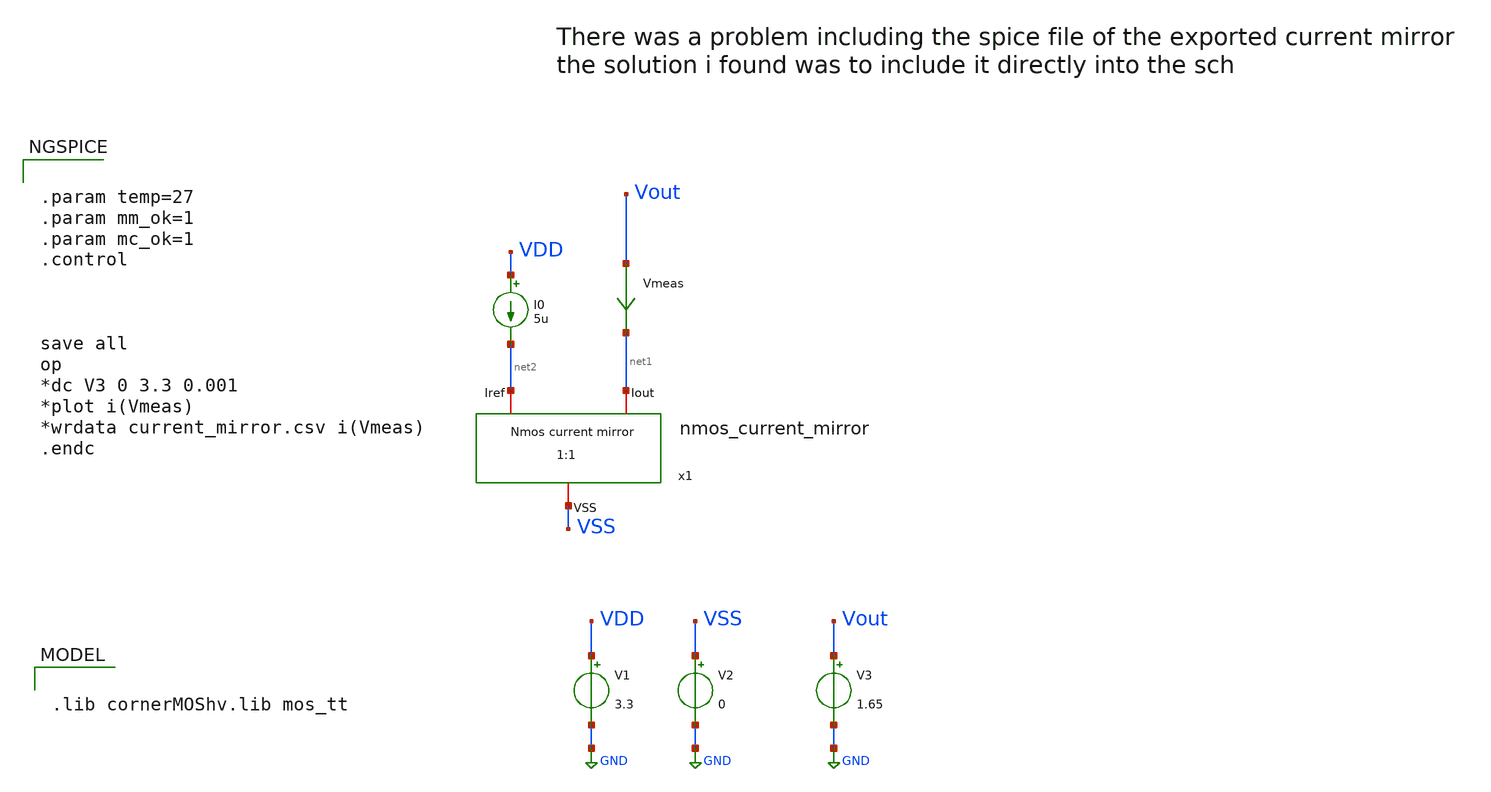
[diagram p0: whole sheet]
** sch_path: Learning/Current_mirrors/Design_nmos_current_mirror_ihp_3_3V/simulations/current_mirror_tb_.sch
**.subckt current_mirror_tb_
V1 VDD GND 3.3
V2 VSS GND 0
I0 VDD net2 5u
Vmeas Vout net1 0
.save i(vmeas)
V3 Vout GND 1.65
x1 VSS net2 net1 nmos_current_mirror
**** begin user architecture code

.lib cornerMOShv.lib mos_tt



.param temp=27
.param mm_ok=1
.param mc_ok=1
.control



save all
op
*dc V3 0 3.3 0.001
*plot i(Vmeas)
*wrdata current_mirror.csv i(Vmeas)
.endc






**** end user architecture code
**.ends
.GLOBAL GND
.end
